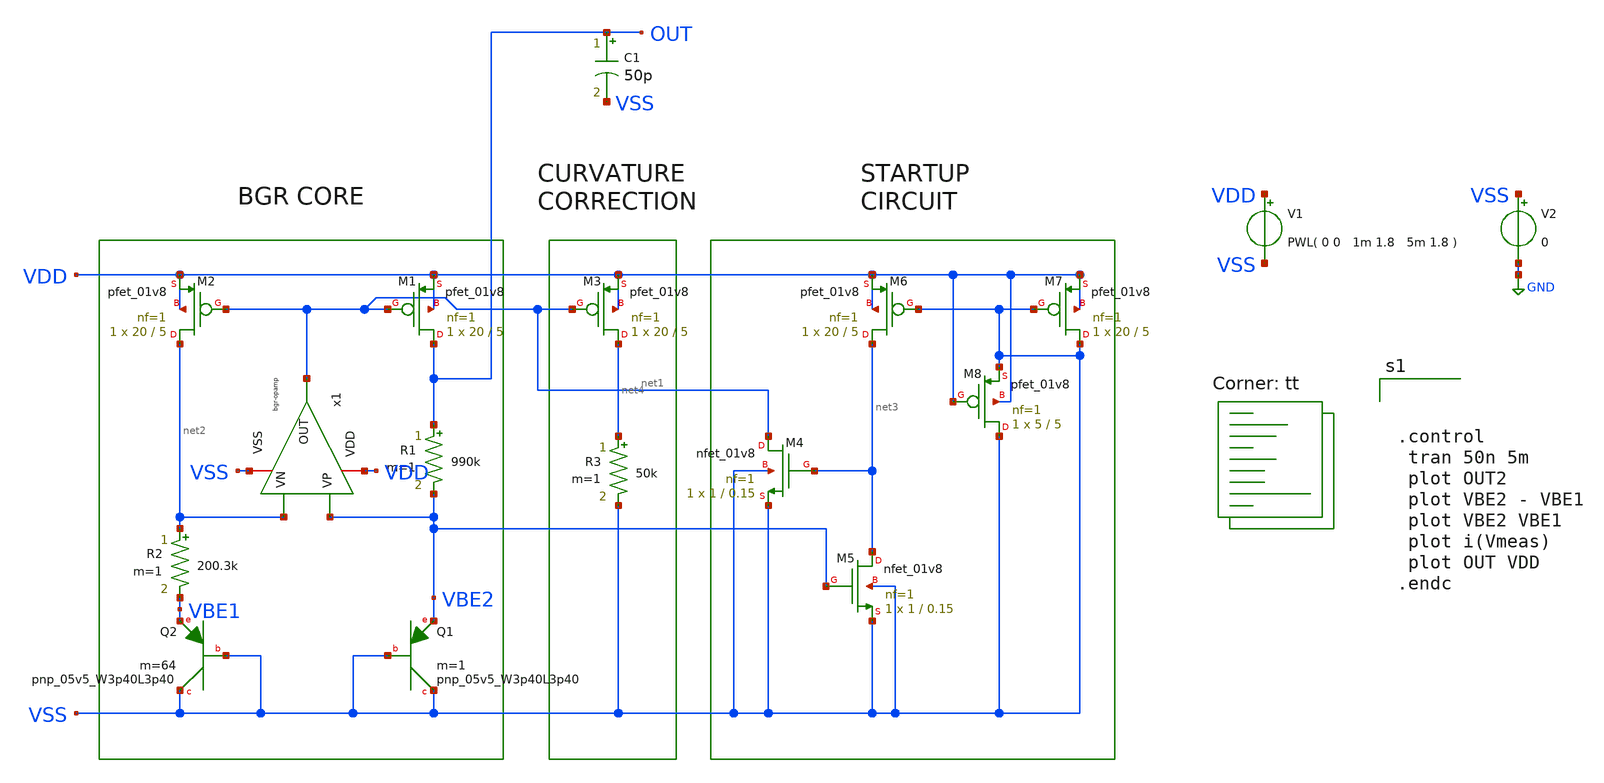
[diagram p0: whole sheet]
** sch_path: bandgap/bgr2-tran.sch
**.subckt bgr2-tran
x1 VDD net1 VBE2 net2 VSS bgr-opamp
XM1 OUT net1 VDD VDD sky130_fd_pr__pfet_01v8 L=5 W=20 nf=1 ad='int((nf+1)/2) * W/nf * 0.29' as='int((nf+2)/2) * W/nf * 0.29'
+ pd='2*int((nf+1)/2) * (W/nf + 0.29)' ps='2*int((nf+2)/2) * (W/nf + 0.29)' nrd='0.29 / W' nrs='0.29 / W'
+ sa=0 sb=0 sd=0 mult=1 m=1
XM2 net2 net1 VDD VDD sky130_fd_pr__pfet_01v8 L=5 W=20 nf=1 ad='int((nf+1)/2) * W/nf * 0.29' as='int((nf+2)/2) * W/nf * 0.29'
+ pd='2*int((nf+1)/2) * (W/nf + 0.29)' ps='2*int((nf+2)/2) * (W/nf + 0.29)' nrd='0.29 / W' nrs='0.29 / W'
+ sa=0 sb=0 sd=0 mult=1 m=1
R1 OUT VBE2 990k m=1
R2 net2 VBE1 200.3k m=1
XQ1 VSS VSS VBE2 sky130_fd_pr__pnp_05v5_W3p40L3p40 m=1
XQ2 VSS VSS VBE1 sky130_fd_pr__pnp_05v5_W3p40L3p40 m=64
V1 VDD VSS PWL( 0 0 1m 1.8 5m 1.8 )
V2 VSS GND 0
XM3 net4 net1 VDD VDD sky130_fd_pr__pfet_01v8 L=5 W=20 nf=1 ad='int((nf+1)/2) * W/nf * 0.29' as='int((nf+2)/2) * W/nf * 0.29'
+ pd='2*int((nf+1)/2) * (W/nf + 0.29)' ps='2*int((nf+2)/2) * (W/nf + 0.29)' nrd='0.29 / W' nrs='0.29 / W'
+ sa=0 sb=0 sd=0 mult=1 m=1
R3 net4 VSS 50k m=1
XM4 net1 net3 VSS VSS sky130_fd_pr__nfet_01v8 L=0.15 W=1 nf=1 ad='int((nf+1)/2) * W/nf * 0.29' as='int((nf+2)/2) * W/nf * 0.29'
+ pd='2*int((nf+1)/2) * (W/nf + 0.29)' ps='2*int((nf+2)/2) * (W/nf + 0.29)' nrd='0.29 / W' nrs='0.29 / W'
+ sa=0 sb=0 sd=0 mult=1 m=1
XM5 net3 VBE2 VSS VSS sky130_fd_pr__nfet_01v8 L=0.15 W=1 nf=1 ad='int((nf+1)/2) * W/nf * 0.29' as='int((nf+2)/2) * W/nf * 0.29'
+ pd='2*int((nf+1)/2) * (W/nf + 0.29)' ps='2*int((nf+2)/2) * (W/nf + 0.29)' nrd='0.29 / W' nrs='0.29 / W'
+ sa=0 sb=0 sd=0 mult=1 m=1
XM6 net3 VSS VDD VDD sky130_fd_pr__pfet_01v8 L=5 W=20 nf=1 ad='int((nf+1)/2) * W/nf * 0.29' as='int((nf+2)/2) * W/nf * 0.29'
+ pd='2*int((nf+1)/2) * (W/nf + 0.29)' ps='2*int((nf+2)/2) * (W/nf + 0.29)' nrd='0.29 / W' nrs='0.29 / W'
+ sa=0 sb=0 sd=0 mult=1 m=1
XM7 VSS VSS VDD VDD sky130_fd_pr__pfet_01v8 L=5 W=20 nf=1 ad='int((nf+1)/2) * W/nf * 0.29' as='int((nf+2)/2) * W/nf * 0.29'
+ pd='2*int((nf+1)/2) * (W/nf + 0.29)' ps='2*int((nf+2)/2) * (W/nf + 0.29)' nrd='0.29 / W' nrs='0.29 / W'
+ sa=0 sb=0 sd=0 mult=1 m=1
XM8 VSS VDD VSS VDD sky130_fd_pr__pfet_01v8 L=5 W=5 nf=1 ad='int((nf+1)/2) * W/nf * 0.29' as='int((nf+2)/2) * W/nf * 0.29'
+ pd='2*int((nf+1)/2) * (W/nf + 0.29)' ps='2*int((nf+2)/2) * (W/nf + 0.29)' nrd='0.29 / W' nrs='0.29 / W'
+ sa=0 sb=0 sd=0 mult=1 m=1
C1 OUT VSS 50p m=1
**** begin user architecture code
.lib $::SKYWATER_MODELS/sky130.lib.spice tt



.control
 tran 50n 5m
 plot OUT2
 plot VBE2 - VBE1
 plot VBE2 VBE1
 plot i(Vmeas)
 plot OUT VDD
.endc


**** end user architecture code
**.ends
.GLOBAL GND
.end
